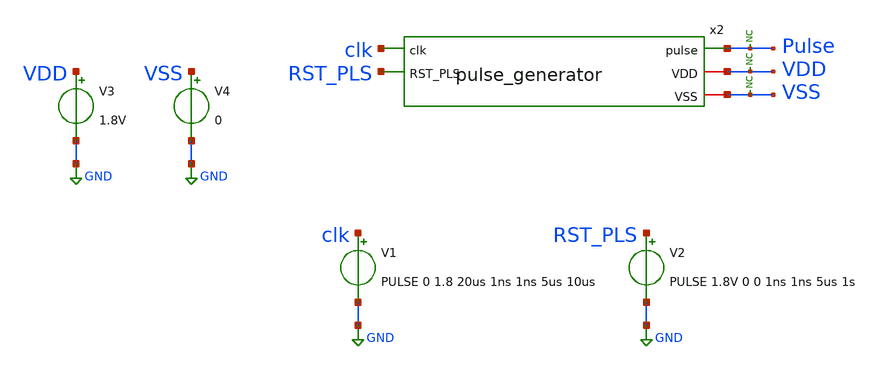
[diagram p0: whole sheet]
** sch_path: xschem/tests/pulse_generator/pulse_generator_test.sch
**.subckt pulse_generator_test
V1 clk GND PULSE 0 1.8 20us 1ns 1ns 5us 10us
V2 RST_PLS GND PULSE 1.8V 0 0 1ns 1ns 5us 1s
* noconn Pulse
* noconn VDD
* noconn VSS
x2 clk Pulse VDD VSS RST_PLS pulse_generator
V3 VDD GND 1.8V
V4 VSS GND 0
**** begin user architecture code
 .lib $::SKYWATER_MODELS/sky130.lib.spice tt
.include $::SKYWATER_STDCELLS/sky130_fd_sc_hd.spice



.options acct list
.temp 25
*vvcc VDD 0 dc 1.8
*vvss VSS 0 0
.control
tran 0.1u 400u
plot RST_PLS clk+2 Pulse+4
write pulse_generator_test.raw
.endc


**** end user architecture code
**.ends

* expanding   symbol:  src/pulse_generator/pulse_generator.sym # of pins=5
** sym_path: xschem/src/pulse_generator/pulse_generator.sym
** sch_path: xschem/src/pulse_generator/pulse_generator.sch
.subckt pulse_generator clk pulse VDD VSS RST_PLS
*.ipin clk
*.ipin RST_PLS
*.opin pulse
*.iopin VDD
*.iopin VSS
x1 clk net1 RST_PLS VSS VSS VDD VDD clk2 net1 sky130_fd_sc_hd__dfrbp_1
x2 clk2 net2 RST_PLS VSS VSS VDD VDD clk4 net2 sky130_fd_sc_hd__dfrbp_1
x3 clk4 net3 RST_PLS VSS VSS VDD VDD clk8 net3 sky130_fd_sc_hd__dfrbp_1
x4 clk8 net4 RST_PLS VSS VSS VDD VDD clk16 net4 sky130_fd_sc_hd__dfrbp_1
x5 delayed clk64 VSS VSS VDD VDD net7 sky130_fd_sc_hd__xor2_1
x9 clk16 net5 RST_PLS VSS VSS VDD VDD clk32 net5 sky130_fd_sc_hd__dfrbp_1
x10 clk32 net6 RST_PLS VSS VSS VDD VDD clk64 net6 sky130_fd_sc_hd__dfrbp_1
* noconn pulse
x6 clk clk64 RST_PLS VSS VSS VDD VDD delayed sky130_fd_sc_hd__dfrtp_1
x7 clk net7 RST_PLS VSS VSS VDD VDD pulse sky130_fd_sc_hd__dfrtn_1
.ends

.GLOBAL GND
.end
